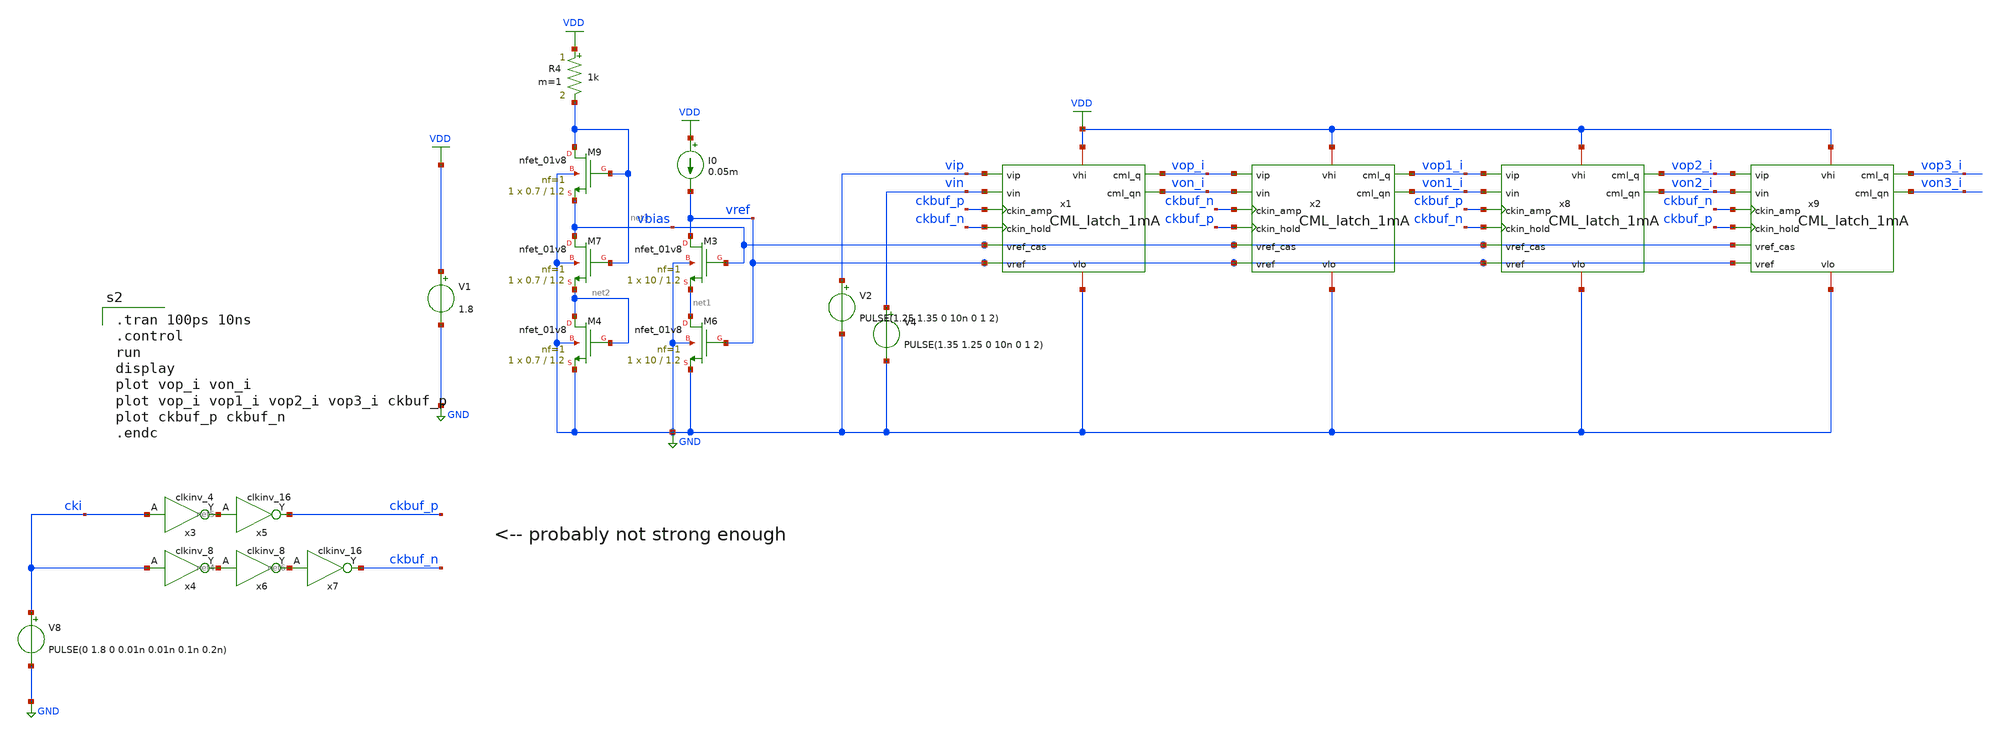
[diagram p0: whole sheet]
** sch_path: xschem/CML_latch_1mA_transient_tb.sch
**.subckt CML_latch_1mA_transient_tb
V1 VDD GND 1.8
XM6 net1 vref GND GND sky130_fd_pr__nfet_01v8 L=1.2 W=10 nf=1 ad='int((nf+1)/2) * W/nf * 0.29' as='int((nf+2)/2) * W/nf * 0.29'
+ pd='2*int((nf+1)/2) * (W/nf + 0.29)' ps='2*int((nf+2)/2) * (W/nf + 0.29)' nrd='0.29 / W' nrs='0.29 / W'
+ sa=0 sb=0 sd=0 mult=1 m=1
I0 VDD vref 0.05m
XM3 vref vbias net1 GND sky130_fd_pr__nfet_01v8 L=1.2 W=10 nf=1 ad='int((nf+1)/2) * W/nf * 0.29' as='int((nf+2)/2) * W/nf * 0.29'
+ pd='2*int((nf+1)/2) * (W/nf + 0.29)' ps='2*int((nf+2)/2) * (W/nf + 0.29)' nrd='0.29 / W' nrs='0.29 / W'
+ sa=0 sb=0 sd=0 mult=1 m=1
XM4 net2 net2 GND GND sky130_fd_pr__nfet_01v8 L=1.2 W=0.7 nf=1 ad='int((nf+1)/2) * W/nf * 0.29' as='int((nf+2)/2) * W/nf * 0.29'
+ pd='2*int((nf+1)/2) * (W/nf + 0.29)' ps='2*int((nf+2)/2) * (W/nf + 0.29)' nrd='0.29 / W' nrs='0.29 / W'
+ sa=0 sb=0 sd=0 mult=1 m=1
XM7 vbias net3 net2 GND sky130_fd_pr__nfet_01v8 L=1.2 W=0.7 nf=1 ad='int((nf+1)/2) * W/nf * 0.29' as='int((nf+2)/2) * W/nf * 0.29'
+ pd='2*int((nf+1)/2) * (W/nf + 0.29)' ps='2*int((nf+2)/2) * (W/nf + 0.29)' nrd='0.29 / W' nrs='0.29 / W'
+ sa=0 sb=0 sd=0 mult=1 m=1
XM9 net3 net3 vbias GND sky130_fd_pr__nfet_01v8 L=1.2 W=0.7 nf=1 ad='int((nf+1)/2) * W/nf * 0.29' as='int((nf+2)/2) * W/nf * 0.29'
+ pd='2*int((nf+1)/2) * (W/nf + 0.29)' ps='2*int((nf+2)/2) * (W/nf + 0.29)' nrd='0.29 / W' nrs='0.29 / W'
+ sa=0 sb=0 sd=0 mult=1 m=1
R4 VDD net3 1k m=1
V8 cki GND PULSE(0 1.8 0 0.01n 0.01n 0.1n 0.2n)
x4 cki gnd gnd vdd vdd net4 sky130_fd_sc_hs__clkinv_8
x3 cki gnd gnd vdd vdd net5 sky130_fd_sc_hs__clkinv_4
x5 net5 gnd gnd vdd vdd ckbuf_p sky130_fd_sc_hs__clkinv_16
x6 net4 gnd gnd vdd vdd net6 sky130_fd_sc_hs__clkinv_8
x7 net6 gnd gnd vdd vdd ckbuf_n sky130_fd_sc_hs__clkinv_16
V4 vin GND PULSE(1.35 1.25 0 10n 0 1 2)
x1 VDD vop_i von_i vip vin ckbuf_p ckbuf_n vbias vref GND CML_latch_1mA
V2 vip GND PULSE(1.25 1.35 0 10n 0 1 2)
x2 VDD vop1_i von1_i vop_i von_i ckbuf_n ckbuf_p vbias vref GND CML_latch_1mA
x8 VDD vop2_i von2_i vop1_i von1_i ckbuf_p ckbuf_n vbias vref GND CML_latch_1mA
x9 VDD vop3_i von3_i vop2_i von2_i ckbuf_n ckbuf_p vbias vref GND CML_latch_1mA
**** begin user architecture code
.lib $::SKYWATER_MODELS/sky130.lib.spice tt
.include $::PDKPATH/libs.ref/sky130_fd_sc_hs/spice/sky130_fd_sc_hs.spice


.tran 100ps 10ns
.control
run
display
plot vop_i von_i
plot vop_i vop1_i vop2_i vop3_i ckbuf_p
plot ckbuf_p ckbuf_n
.endc


**** end user architecture code
**.ends

* expanding   symbol:  CML_latch_1mA.sym # of pins=10
** sym_path: xschem/CML_latch_1mA.sym
** sch_path: xschem/CML_latch_1mA.sch
.subckt CML_latch_1mA vhi cml_q cml_qn vip vin ckin_amp ckin_hold vref_cas vref vlo
*.opin cml_q
*.opin cml_qn
*.iopin vhi
*.ipin ckin_amp
*.ipin ckin_hold
*.ipin vref_cas
*.ipin vref
*.iopin vlo
*.ipin vip
*.ipin vin
XM5 net1 vref vlo vlo sky130_fd_pr__nfet_01v8 L=1.2 W=10 nf=1 ad='int((nf+1)/2) * W/nf * 0.29' as='int((nf+2)/2) * W/nf * 0.29'
+ pd='2*int((nf+1)/2) * (W/nf + 0.29)' ps='2*int((nf+2)/2) * (W/nf + 0.29)' nrd='0.29 / W' nrs='0.29 / W'
+ sa=0 sb=0 sd=0 mult=20 m=20
XM2 vcenter vref_cas net1 vlo sky130_fd_pr__nfet_01v8 L=1.2 W=10 nf=1 ad='int((nf+1)/2) * W/nf * 0.29'
+ as='int((nf+2)/2) * W/nf * 0.29' pd='2*int((nf+1)/2) * (W/nf + 0.29)' ps='2*int((nf+2)/2) * (W/nf + 0.29)'
+ nrd='0.29 / W' nrs='0.29 / W' sa=0 sb=0 sd=0 mult=20 m=20
XM1 vmid_amp ckin_amp vcenter vlo sky130_fd_pr__nfet_01v8 L=0.15 W=20 nf=1 ad='int((nf+1)/2) * W/nf * 0.29'
+ as='int((nf+2)/2) * W/nf * 0.29' pd='2*int((nf+1)/2) * (W/nf + 0.29)' ps='2*int((nf+2)/2) * (W/nf + 0.29)'
+ nrd='0.29 / W' nrs='0.29 / W' sa=0 sb=0 sd=0 mult=1 m=1
XM8 vmid_hold ckin_hold vcenter vlo sky130_fd_pr__nfet_01v8 L=0.15 W=20 nf=1 ad='int((nf+1)/2) * W/nf * 0.29'
+ as='int((nf+2)/2) * W/nf * 0.29' pd='2*int((nf+1)/2) * (W/nf + 0.29)' ps='2*int((nf+2)/2) * (W/nf + 0.29)'
+ nrd='0.29 / W' nrs='0.29 / W' sa=0 sb=0 sd=0 mult=1 m=1
XM10 cml_qn vip vmid_amp vlo sky130_fd_pr__nfet_01v8 L=0.15 W=20 nf=1 ad='int((nf+1)/2) * W/nf * 0.29'
+ as='int((nf+2)/2) * W/nf * 0.29' pd='2*int((nf+1)/2) * (W/nf + 0.29)' ps='2*int((nf+2)/2) * (W/nf + 0.29)'
+ nrd='0.29 / W' nrs='0.29 / W' sa=0 sb=0 sd=0 mult=1 m=1
XM11 cml_q vin vmid_amp vlo sky130_fd_pr__nfet_01v8 L=0.15 W=20 nf=1 ad='int((nf+1)/2) * W/nf * 0.29'
+ as='int((nf+2)/2) * W/nf * 0.29' pd='2*int((nf+1)/2) * (W/nf + 0.29)' ps='2*int((nf+2)/2) * (W/nf + 0.29)'
+ nrd='0.29 / W' nrs='0.29 / W' sa=0 sb=0 sd=0 mult=1 m=1
XM12 cml_q cml_qn vmid_hold vlo sky130_fd_pr__nfet_01v8 L=0.15 W=10 nf=1 ad='int((nf+1)/2) * W/nf * 0.29'
+ as='int((nf+2)/2) * W/nf * 0.29' pd='2*int((nf+1)/2) * (W/nf + 0.29)' ps='2*int((nf+2)/2) * (W/nf + 0.29)'
+ nrd='0.29 / W' nrs='0.29 / W' sa=0 sb=0 sd=0 mult=1 m=1
XM13 cml_qn cml_q vmid_hold vlo sky130_fd_pr__nfet_01v8 L=0.15 W=10 nf=1 ad='int((nf+1)/2) * W/nf * 0.29'
+ as='int((nf+2)/2) * W/nf * 0.29' pd='2*int((nf+1)/2) * (W/nf + 0.29)' ps='2*int((nf+2)/2) * (W/nf + 0.29)'
+ nrd='0.29 / W' nrs='0.29 / W' sa=0 sb=0 sd=0 mult=1 m=1
R1 vhi cml_qn 1k m=1
R2 vhi cml_q 1k m=1
.ends

.GLOBAL GND
.GLOBAL VDD
.end
